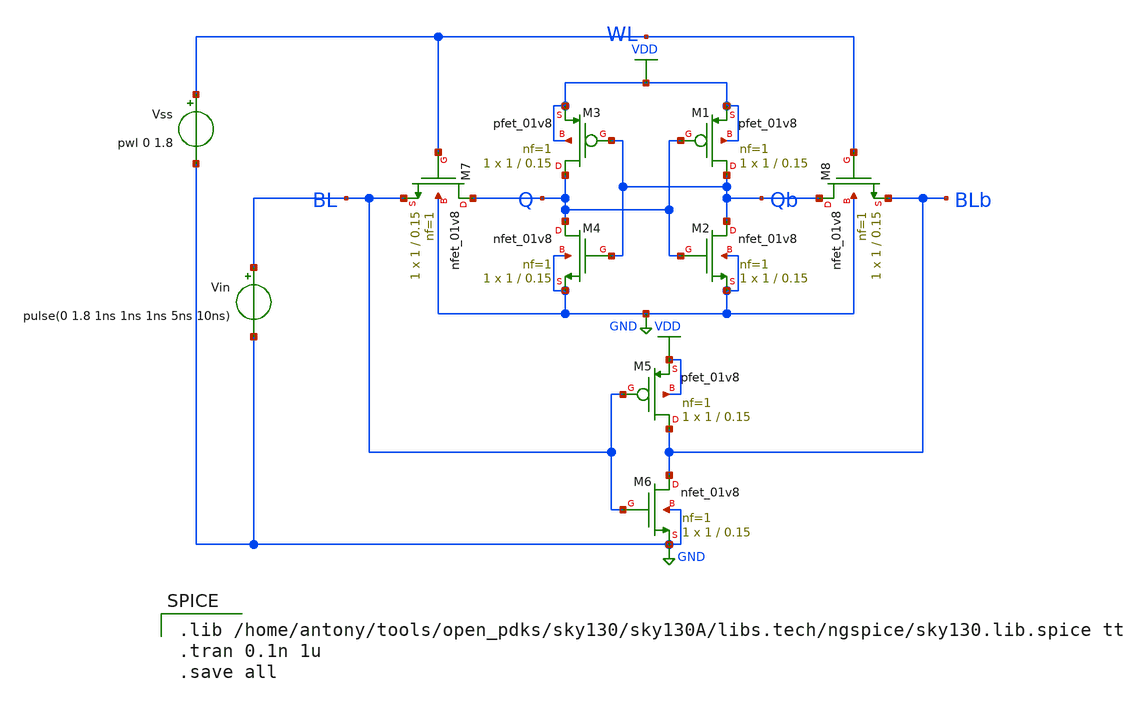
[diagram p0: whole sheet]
** sch_path: 6t_sram_130.sch
**.subckt 6t_sram_130
Vin BL GND pulse(0 1.8 1ns 1ns 1ns 5ns 10ns)
Vss WL GND pwl 0 1.8
XM1 Qb Q VDD VDD sky130_fd_pr__pfet_01v8 L=0.15 W=1 nf=1 ad='int((nf+1)/2) * W/nf * 0.29' as='int((nf+2)/2) * W/nf * 0.29'
+ pd='2*int((nf+1)/2) * (W/nf + 0.29)' ps='2*int((nf+2)/2) * (W/nf + 0.29)' nrd='0.29 / W' nrs='0.29 / W'
+ sa=0 sb=0 sd=0 mult=1 m=1
XM2 Qb Q GND GND sky130_fd_pr__nfet_01v8 L=0.15 W=1 nf=1 ad='int((nf+1)/2) * W/nf * 0.29' as='int((nf+2)/2) * W/nf * 0.29'
+ pd='2*int((nf+1)/2) * (W/nf + 0.29)' ps='2*int((nf+2)/2) * (W/nf + 0.29)' nrd='0.29 / W' nrs='0.29 / W'
+ sa=0 sb=0 sd=0 mult=1 m=1
XM3 Q Qb VDD VDD sky130_fd_pr__pfet_01v8 L=0.15 W=1 nf=1 ad='int((nf+1)/2) * W/nf * 0.29' as='int((nf+2)/2) * W/nf * 0.29'
+ pd='2*int((nf+1)/2) * (W/nf + 0.29)' ps='2*int((nf+2)/2) * (W/nf + 0.29)' nrd='0.29 / W' nrs='0.29 / W'
+ sa=0 sb=0 sd=0 mult=1 m=1
XM4 Q Qb GND GND sky130_fd_pr__nfet_01v8 L=0.15 W=1 nf=1 ad='int((nf+1)/2) * W/nf * 0.29' as='int((nf+2)/2) * W/nf * 0.29'
+ pd='2*int((nf+1)/2) * (W/nf + 0.29)' ps='2*int((nf+2)/2) * (W/nf + 0.29)' nrd='0.29 / W' nrs='0.29 / W'
+ sa=0 sb=0 sd=0 mult=1 m=1
XM5 BLb BL VDD VDD sky130_fd_pr__pfet_01v8 L=0.15 W=1 nf=1 ad='int((nf+1)/2) * W/nf * 0.29' as='int((nf+2)/2) * W/nf * 0.29'
+ pd='2*int((nf+1)/2) * (W/nf + 0.29)' ps='2*int((nf+2)/2) * (W/nf + 0.29)' nrd='0.29 / W' nrs='0.29 / W'
+ sa=0 sb=0 sd=0 mult=1 m=1
XM6 BLb BL GND GND sky130_fd_pr__nfet_01v8 L=0.15 W=1 nf=1 ad='int((nf+1)/2) * W/nf * 0.29' as='int((nf+2)/2) * W/nf * 0.29'
+ pd='2*int((nf+1)/2) * (W/nf + 0.29)' ps='2*int((nf+2)/2) * (W/nf + 0.29)' nrd='0.29 / W' nrs='0.29 / W'
+ sa=0 sb=0 sd=0 mult=1 m=1
XM7 Q WL BL GND sky130_fd_pr__nfet_01v8 L=0.15 W=1 nf=1 ad='int((nf+1)/2) * W/nf * 0.29' as='int((nf+2)/2) * W/nf * 0.29'
+ pd='2*int((nf+1)/2) * (W/nf + 0.29)' ps='2*int((nf+2)/2) * (W/nf + 0.29)' nrd='0.29 / W' nrs='0.29 / W'
+ sa=0 sb=0 sd=0 mult=1 m=1
XM8 Qb WL BLb GND sky130_fd_pr__nfet_01v8 L=0.15 W=1 nf=1 ad='int((nf+1)/2) * W/nf * 0.29' as='int((nf+2)/2) * W/nf * 0.29'
+ pd='2*int((nf+1)/2) * (W/nf + 0.29)' ps='2*int((nf+2)/2) * (W/nf + 0.29)' nrd='0.29 / W' nrs='0.29 / W'
+ sa=0 sb=0 sd=0 mult=1 m=1
**** begin user architecture code

.lib /home/antony/tools/open_pdks/sky130/sky130A/libs.tech/ngspice/sky130.lib.spice tt
.tran 0.1n 1u
.save all

**** end user architecture code
**.ends
.GLOBAL VDD
.GLOBAL GND
.end
